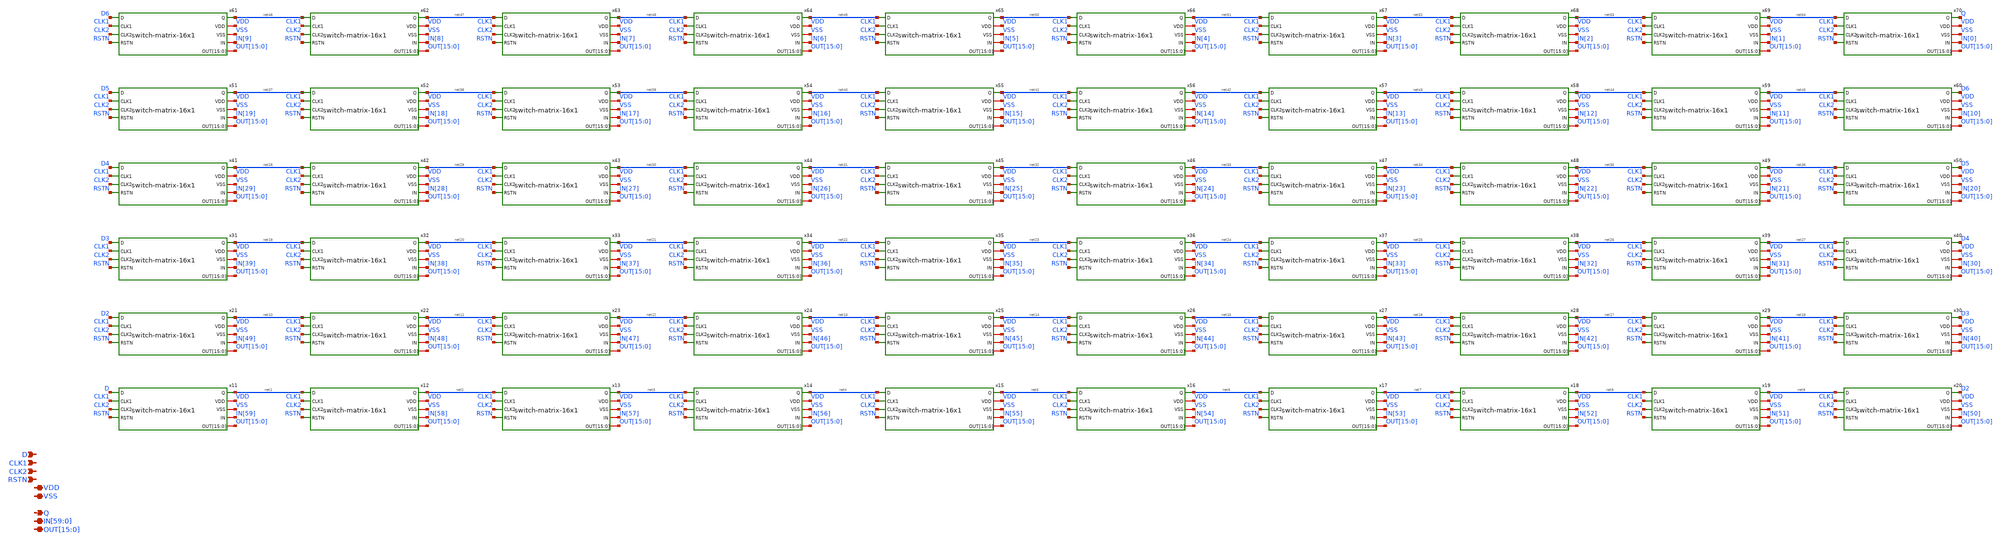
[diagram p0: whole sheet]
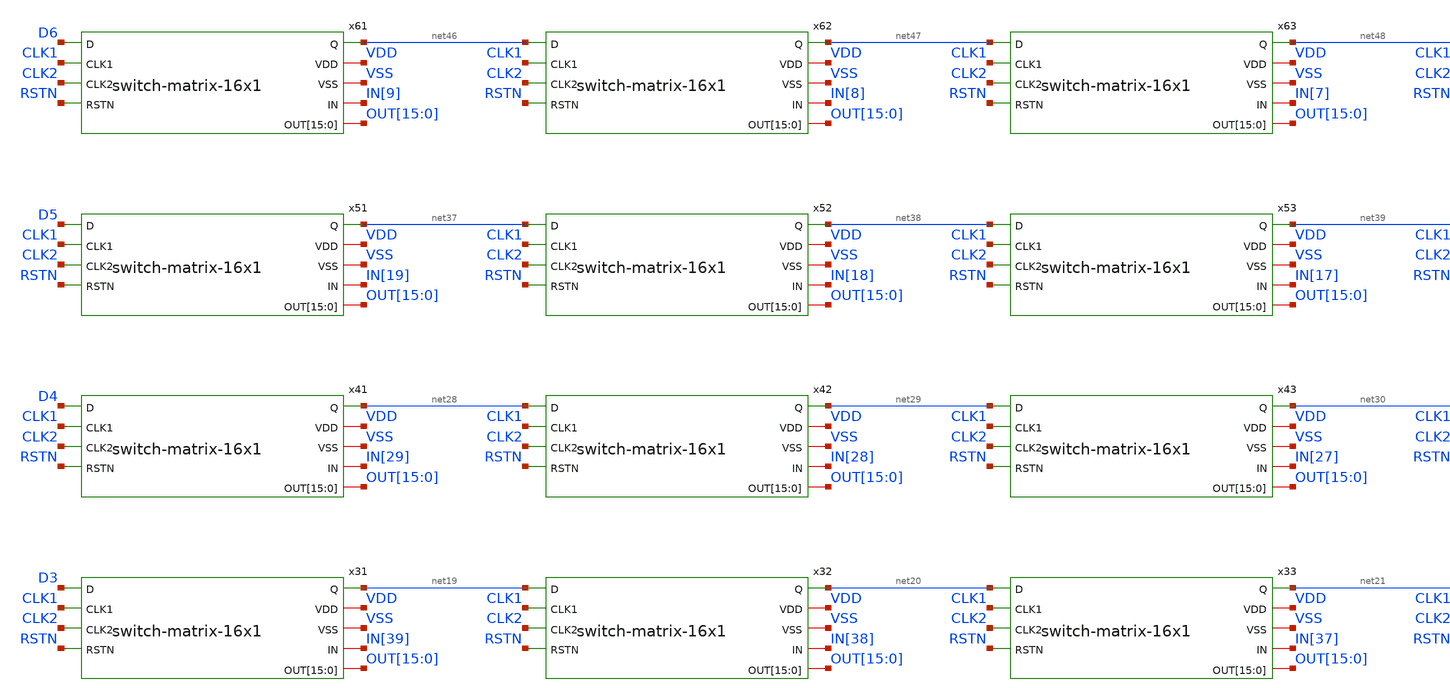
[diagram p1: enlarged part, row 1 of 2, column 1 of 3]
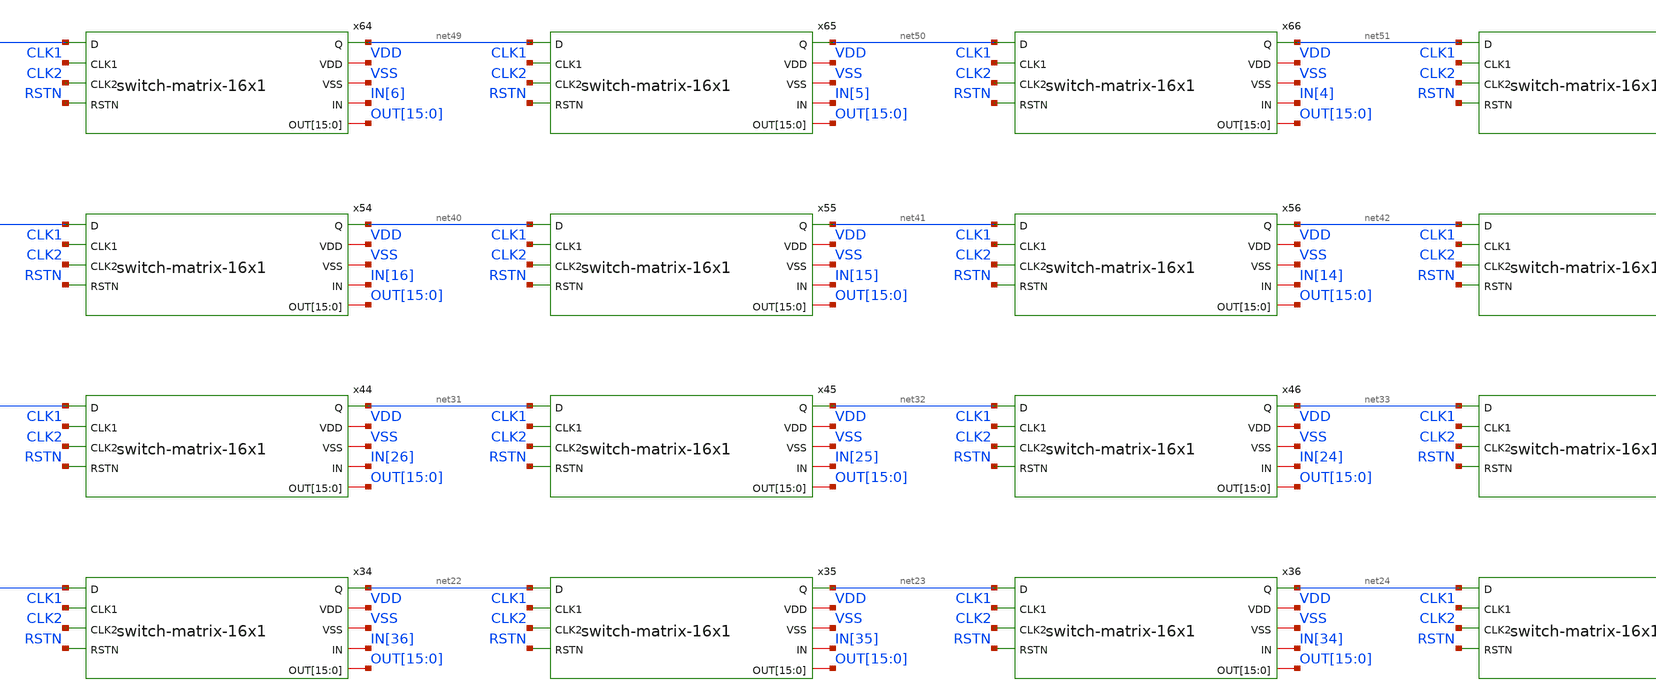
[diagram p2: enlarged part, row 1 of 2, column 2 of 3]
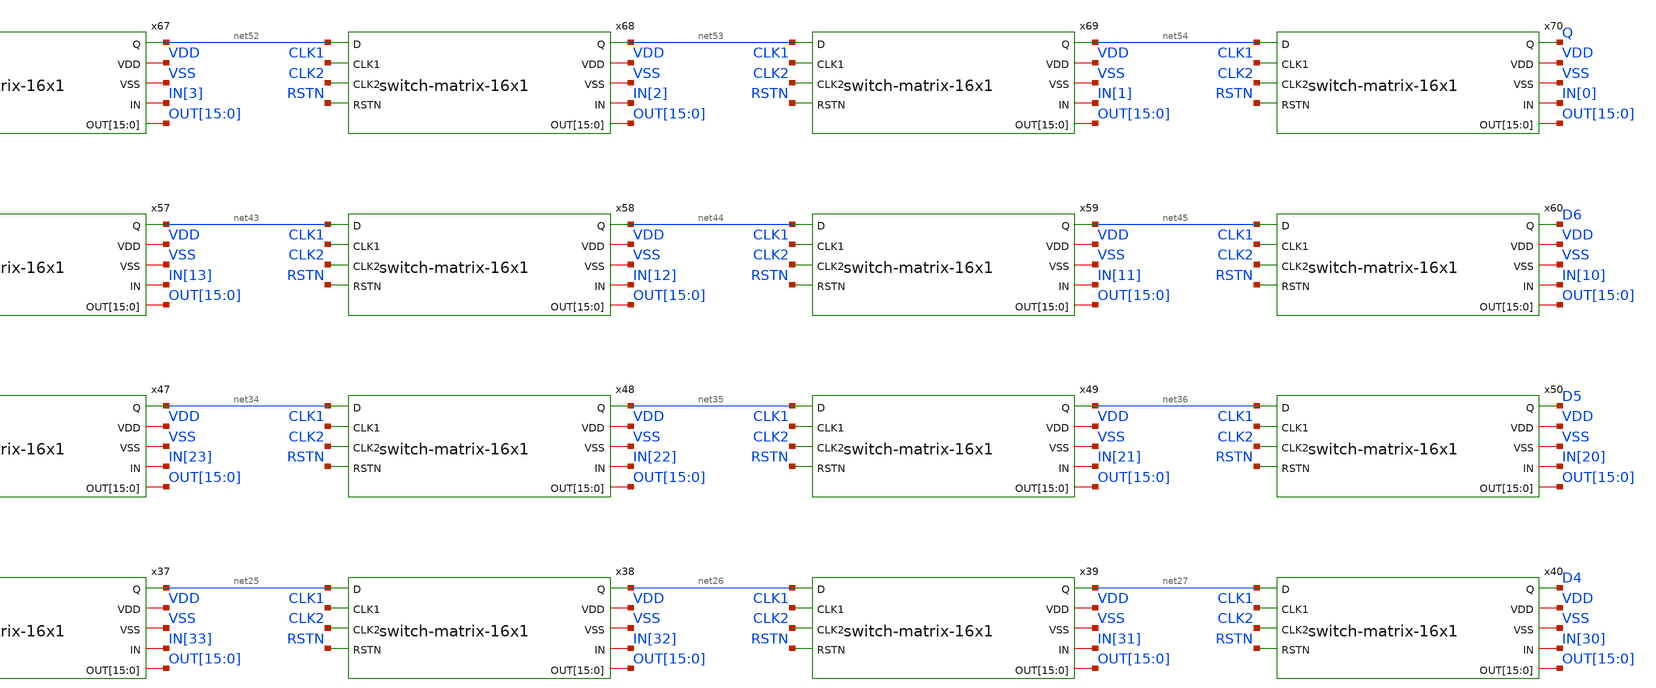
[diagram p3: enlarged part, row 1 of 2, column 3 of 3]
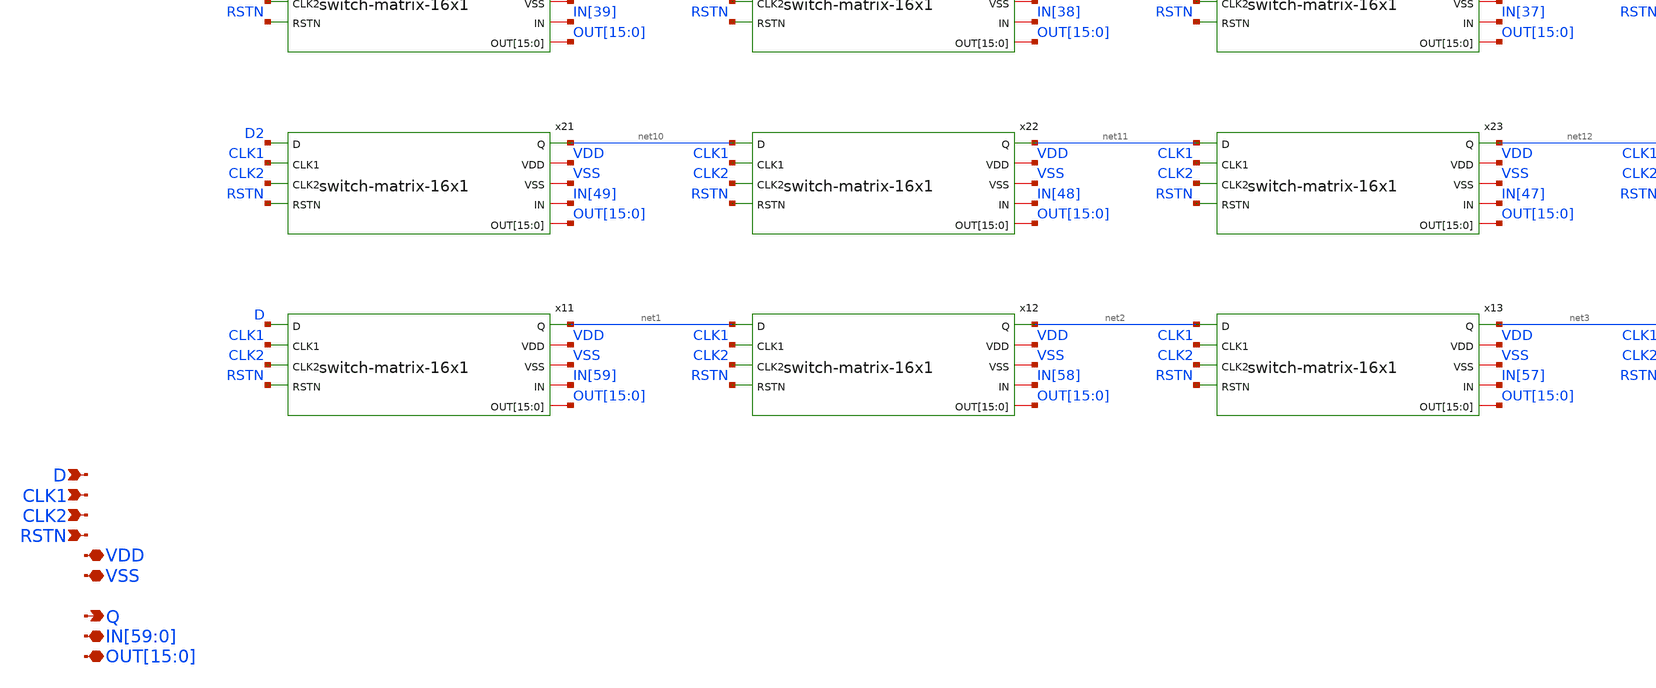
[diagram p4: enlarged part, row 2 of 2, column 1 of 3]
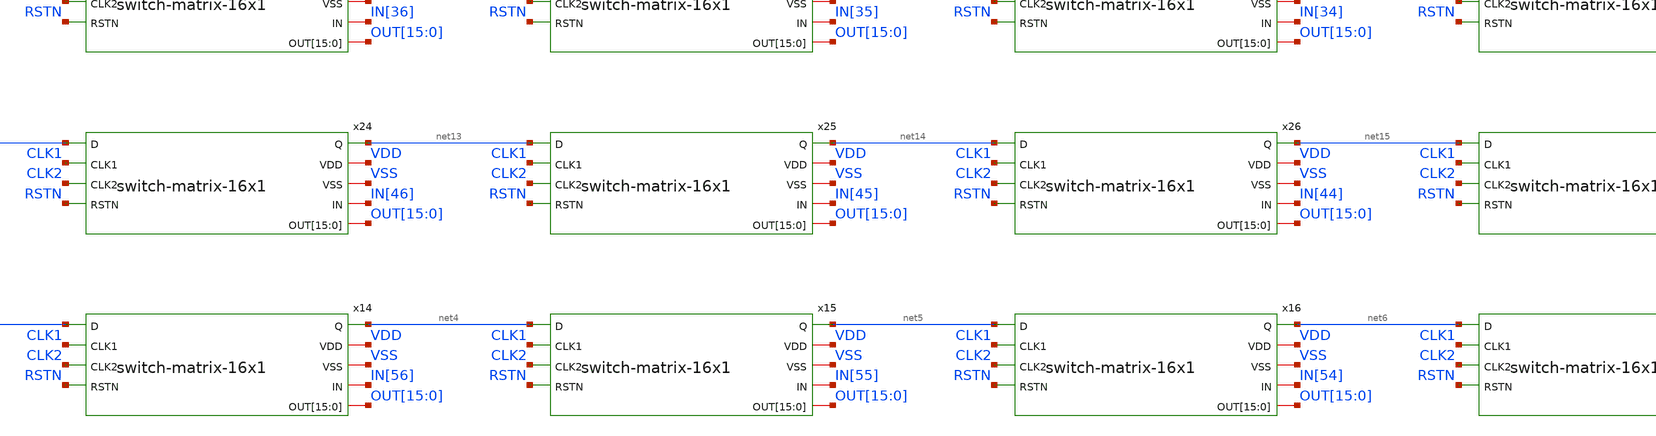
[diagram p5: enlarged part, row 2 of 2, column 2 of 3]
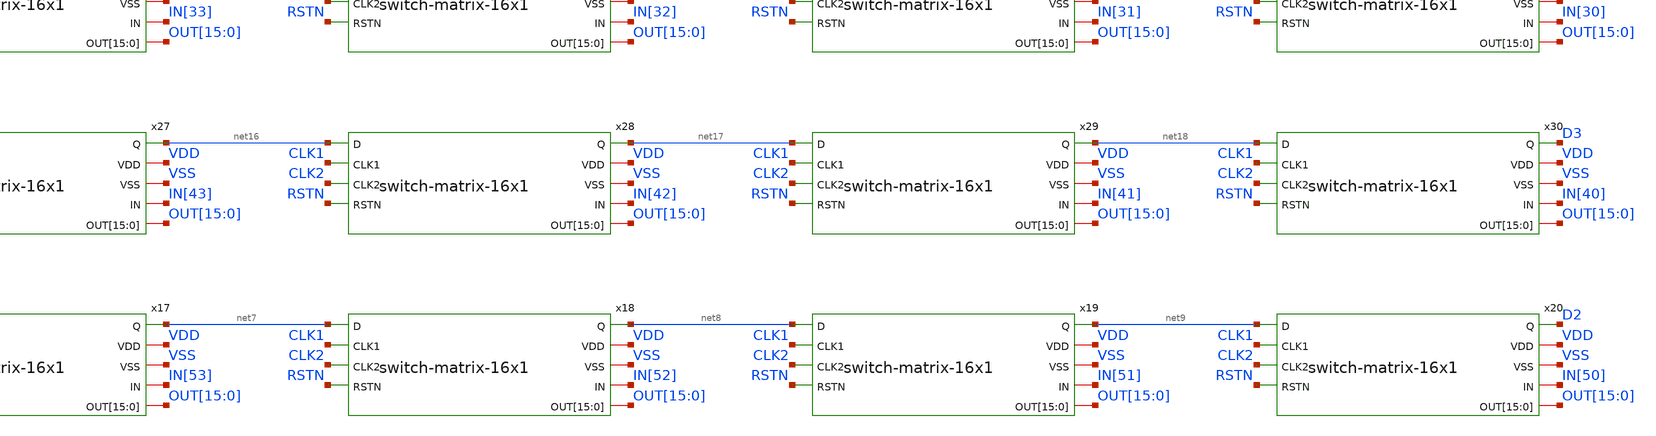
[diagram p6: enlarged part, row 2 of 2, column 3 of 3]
** sch_path: designs/libs/core_switch-matrix/switch-matrix-16x70/switch-matrix-16x70.sch
**.subckt switch-matrix-16x70 VDD VSS RSTN CLK1 CLK2 D
*+ IN[59],IN[58],IN[57],IN[56],IN[55],IN[54],IN[53],IN[52],IN[51],IN[50],IN[49],IN[48],IN[47],IN[46],IN[45],IN[44],IN[43],IN[42],IN[41],IN[40],IN[39],IN[38],IN[37],IN[36],IN[35],IN[34],IN[33],IN[32],IN[31],IN[30],IN[29],IN[28],IN[27],IN[26],IN[25],IN[24],IN[23],IN[22],IN[21],IN[20],IN[19],IN[18],IN[17],IN[16],IN[15],IN[14],IN[13],IN[12],IN[11],IN[10],IN[9],IN[8],IN[7],IN[6],IN[5],IN[4],IN[3],IN[2],IN[1],IN[0]
*+ OUT[15],OUT[14],OUT[13],OUT[12],OUT[11],OUT[10],OUT[9],OUT[8],OUT[7],OUT[6],OUT[5],OUT[4],OUT[3],OUT[2],OUT[1],OUT[0] Q
*.iopin VDD
*.iopin VSS
*.ipin RSTN
*.ipin CLK1
*.ipin CLK2
*.ipin D
*.iopin
*+ IN[59],IN[58],IN[57],IN[56],IN[55],IN[54],IN[53],IN[52],IN[51],IN[50],IN[49],IN[48],IN[47],IN[46],IN[45],IN[44],IN[43],IN[42],IN[41],IN[40],IN[39],IN[38],IN[37],IN[36],IN[35],IN[34],IN[33],IN[32],IN[31],IN[30],IN[29],IN[28],IN[27],IN[26],IN[25],IN[24],IN[23],IN[22],IN[21],IN[20],IN[19],IN[18],IN[17],IN[16],IN[15],IN[14],IN[13],IN[12],IN[11],IN[10],IN[9],IN[8],IN[7],IN[6],IN[5],IN[4],IN[3],IN[2],IN[1],IN[0]
*.iopin
*+ OUT[15],OUT[14],OUT[13],OUT[12],OUT[11],OUT[10],OUT[9],OUT[8],OUT[7],OUT[6],OUT[5],OUT[4],OUT[3],OUT[2],OUT[1],OUT[0]
*.opin Q
x11 net1 VDD VSS IN[59] OUT[15] OUT[14] OUT[13] OUT[12] OUT[11] OUT[10] OUT[9] OUT[8] OUT[7] OUT[6]
+ OUT[5] OUT[4] OUT[3] OUT[2] OUT[1] OUT[0] D CLK1 CLK2 RSTN switch-matrix-16x1
x12 net2 VDD VSS IN[58] OUT[15] OUT[14] OUT[13] OUT[12] OUT[11] OUT[10] OUT[9] OUT[8] OUT[7] OUT[6]
+ OUT[5] OUT[4] OUT[3] OUT[2] OUT[1] OUT[0] net1 CLK1 CLK2 RSTN switch-matrix-16x1
x13 net3 VDD VSS IN[57] OUT[15] OUT[14] OUT[13] OUT[12] OUT[11] OUT[10] OUT[9] OUT[8] OUT[7] OUT[6]
+ OUT[5] OUT[4] OUT[3] OUT[2] OUT[1] OUT[0] net2 CLK1 CLK2 RSTN switch-matrix-16x1
x14 net4 VDD VSS IN[56] OUT[15] OUT[14] OUT[13] OUT[12] OUT[11] OUT[10] OUT[9] OUT[8] OUT[7] OUT[6]
+ OUT[5] OUT[4] OUT[3] OUT[2] OUT[1] OUT[0] net3 CLK1 CLK2 RSTN switch-matrix-16x1
x15 net5 VDD VSS IN[55] OUT[15] OUT[14] OUT[13] OUT[12] OUT[11] OUT[10] OUT[9] OUT[8] OUT[7] OUT[6]
+ OUT[5] OUT[4] OUT[3] OUT[2] OUT[1] OUT[0] net4 CLK1 CLK2 RSTN switch-matrix-16x1
x16 net6 VDD VSS IN[54] OUT[15] OUT[14] OUT[13] OUT[12] OUT[11] OUT[10] OUT[9] OUT[8] OUT[7] OUT[6]
+ OUT[5] OUT[4] OUT[3] OUT[2] OUT[1] OUT[0] net5 CLK1 CLK2 RSTN switch-matrix-16x1
x17 net7 VDD VSS IN[53] OUT[15] OUT[14] OUT[13] OUT[12] OUT[11] OUT[10] OUT[9] OUT[8] OUT[7] OUT[6]
+ OUT[5] OUT[4] OUT[3] OUT[2] OUT[1] OUT[0] net6 CLK1 CLK2 RSTN switch-matrix-16x1
x18 net8 VDD VSS IN[52] OUT[15] OUT[14] OUT[13] OUT[12] OUT[11] OUT[10] OUT[9] OUT[8] OUT[7] OUT[6]
+ OUT[5] OUT[4] OUT[3] OUT[2] OUT[1] OUT[0] net7 CLK1 CLK2 RSTN switch-matrix-16x1
x19 net9 VDD VSS IN[51] OUT[15] OUT[14] OUT[13] OUT[12] OUT[11] OUT[10] OUT[9] OUT[8] OUT[7] OUT[6]
+ OUT[5] OUT[4] OUT[3] OUT[2] OUT[1] OUT[0] net8 CLK1 CLK2 RSTN switch-matrix-16x1
x20 D2 VDD VSS IN[50] OUT[15] OUT[14] OUT[13] OUT[12] OUT[11] OUT[10] OUT[9] OUT[8] OUT[7] OUT[6]
+ OUT[5] OUT[4] OUT[3] OUT[2] OUT[1] OUT[0] net9 CLK1 CLK2 RSTN switch-matrix-16x1
x21 net10 VDD VSS IN[49] OUT[15] OUT[14] OUT[13] OUT[12] OUT[11] OUT[10] OUT[9] OUT[8] OUT[7] OUT[6]
+ OUT[5] OUT[4] OUT[3] OUT[2] OUT[1] OUT[0] D2 CLK1 CLK2 RSTN switch-matrix-16x1
x22 net11 VDD VSS IN[48] OUT[15] OUT[14] OUT[13] OUT[12] OUT[11] OUT[10] OUT[9] OUT[8] OUT[7] OUT[6]
+ OUT[5] OUT[4] OUT[3] OUT[2] OUT[1] OUT[0] net10 CLK1 CLK2 RSTN switch-matrix-16x1
x23 net12 VDD VSS IN[47] OUT[15] OUT[14] OUT[13] OUT[12] OUT[11] OUT[10] OUT[9] OUT[8] OUT[7] OUT[6]
+ OUT[5] OUT[4] OUT[3] OUT[2] OUT[1] OUT[0] net11 CLK1 CLK2 RSTN switch-matrix-16x1
x24 net13 VDD VSS IN[46] OUT[15] OUT[14] OUT[13] OUT[12] OUT[11] OUT[10] OUT[9] OUT[8] OUT[7] OUT[6]
+ OUT[5] OUT[4] OUT[3] OUT[2] OUT[1] OUT[0] net12 CLK1 CLK2 RSTN switch-matrix-16x1
x25 net14 VDD VSS IN[45] OUT[15] OUT[14] OUT[13] OUT[12] OUT[11] OUT[10] OUT[9] OUT[8] OUT[7] OUT[6]
+ OUT[5] OUT[4] OUT[3] OUT[2] OUT[1] OUT[0] net13 CLK1 CLK2 RSTN switch-matrix-16x1
x26 net15 VDD VSS IN[44] OUT[15] OUT[14] OUT[13] OUT[12] OUT[11] OUT[10] OUT[9] OUT[8] OUT[7] OUT[6]
+ OUT[5] OUT[4] OUT[3] OUT[2] OUT[1] OUT[0] net14 CLK1 CLK2 RSTN switch-matrix-16x1
x27 net16 VDD VSS IN[43] OUT[15] OUT[14] OUT[13] OUT[12] OUT[11] OUT[10] OUT[9] OUT[8] OUT[7] OUT[6]
+ OUT[5] OUT[4] OUT[3] OUT[2] OUT[1] OUT[0] net15 CLK1 CLK2 RSTN switch-matrix-16x1
x28 net17 VDD VSS IN[42] OUT[15] OUT[14] OUT[13] OUT[12] OUT[11] OUT[10] OUT[9] OUT[8] OUT[7] OUT[6]
+ OUT[5] OUT[4] OUT[3] OUT[2] OUT[1] OUT[0] net16 CLK1 CLK2 RSTN switch-matrix-16x1
x29 net18 VDD VSS IN[41] OUT[15] OUT[14] OUT[13] OUT[12] OUT[11] OUT[10] OUT[9] OUT[8] OUT[7] OUT[6]
+ OUT[5] OUT[4] OUT[3] OUT[2] OUT[1] OUT[0] net17 CLK1 CLK2 RSTN switch-matrix-16x1
x30 D3 VDD VSS IN[40] OUT[15] OUT[14] OUT[13] OUT[12] OUT[11] OUT[10] OUT[9] OUT[8] OUT[7] OUT[6]
+ OUT[5] OUT[4] OUT[3] OUT[2] OUT[1] OUT[0] net18 CLK1 CLK2 RSTN switch-matrix-16x1
x31 net19 VDD VSS IN[39] OUT[15] OUT[14] OUT[13] OUT[12] OUT[11] OUT[10] OUT[9] OUT[8] OUT[7] OUT[6]
+ OUT[5] OUT[4] OUT[3] OUT[2] OUT[1] OUT[0] D3 CLK1 CLK2 RSTN switch-matrix-16x1
x32 net20 VDD VSS IN[38] OUT[15] OUT[14] OUT[13] OUT[12] OUT[11] OUT[10] OUT[9] OUT[8] OUT[7] OUT[6]
+ OUT[5] OUT[4] OUT[3] OUT[2] OUT[1] OUT[0] net19 CLK1 CLK2 RSTN switch-matrix-16x1
x33 net21 VDD VSS IN[37] OUT[15] OUT[14] OUT[13] OUT[12] OUT[11] OUT[10] OUT[9] OUT[8] OUT[7] OUT[6]
+ OUT[5] OUT[4] OUT[3] OUT[2] OUT[1] OUT[0] net20 CLK1 CLK2 RSTN switch-matrix-16x1
x34 net22 VDD VSS IN[36] OUT[15] OUT[14] OUT[13] OUT[12] OUT[11] OUT[10] OUT[9] OUT[8] OUT[7] OUT[6]
+ OUT[5] OUT[4] OUT[3] OUT[2] OUT[1] OUT[0] net21 CLK1 CLK2 RSTN switch-matrix-16x1
x35 net23 VDD VSS IN[35] OUT[15] OUT[14] OUT[13] OUT[12] OUT[11] OUT[10] OUT[9] OUT[8] OUT[7] OUT[6]
+ OUT[5] OUT[4] OUT[3] OUT[2] OUT[1] OUT[0] net22 CLK1 CLK2 RSTN switch-matrix-16x1
x36 net24 VDD VSS IN[34] OUT[15] OUT[14] OUT[13] OUT[12] OUT[11] OUT[10] OUT[9] OUT[8] OUT[7] OUT[6]
+ OUT[5] OUT[4] OUT[3] OUT[2] OUT[1] OUT[0] net23 CLK1 CLK2 RSTN switch-matrix-16x1
x37 net25 VDD VSS IN[33] OUT[15] OUT[14] OUT[13] OUT[12] OUT[11] OUT[10] OUT[9] OUT[8] OUT[7] OUT[6]
+ OUT[5] OUT[4] OUT[3] OUT[2] OUT[1] OUT[0] net24 CLK1 CLK2 RSTN switch-matrix-16x1
x38 net26 VDD VSS IN[32] OUT[15] OUT[14] OUT[13] OUT[12] OUT[11] OUT[10] OUT[9] OUT[8] OUT[7] OUT[6]
+ OUT[5] OUT[4] OUT[3] OUT[2] OUT[1] OUT[0] net25 CLK1 CLK2 RSTN switch-matrix-16x1
x39 net27 VDD VSS IN[31] OUT[15] OUT[14] OUT[13] OUT[12] OUT[11] OUT[10] OUT[9] OUT[8] OUT[7] OUT[6]
+ OUT[5] OUT[4] OUT[3] OUT[2] OUT[1] OUT[0] net26 CLK1 CLK2 RSTN switch-matrix-16x1
x40 D4 VDD VSS IN[30] OUT[15] OUT[14] OUT[13] OUT[12] OUT[11] OUT[10] OUT[9] OUT[8] OUT[7] OUT[6]
+ OUT[5] OUT[4] OUT[3] OUT[2] OUT[1] OUT[0] net27 CLK1 CLK2 RSTN switch-matrix-16x1
x41 net28 VDD VSS IN[29] OUT[15] OUT[14] OUT[13] OUT[12] OUT[11] OUT[10] OUT[9] OUT[8] OUT[7] OUT[6]
+ OUT[5] OUT[4] OUT[3] OUT[2] OUT[1] OUT[0] D4 CLK1 CLK2 RSTN switch-matrix-16x1
x42 net29 VDD VSS IN[28] OUT[15] OUT[14] OUT[13] OUT[12] OUT[11] OUT[10] OUT[9] OUT[8] OUT[7] OUT[6]
+ OUT[5] OUT[4] OUT[3] OUT[2] OUT[1] OUT[0] net28 CLK1 CLK2 RSTN switch-matrix-16x1
x43 net30 VDD VSS IN[27] OUT[15] OUT[14] OUT[13] OUT[12] OUT[11] OUT[10] OUT[9] OUT[8] OUT[7] OUT[6]
+ OUT[5] OUT[4] OUT[3] OUT[2] OUT[1] OUT[0] net29 CLK1 CLK2 RSTN switch-matrix-16x1
x44 net31 VDD VSS IN[26] OUT[15] OUT[14] OUT[13] OUT[12] OUT[11] OUT[10] OUT[9] OUT[8] OUT[7] OUT[6]
+ OUT[5] OUT[4] OUT[3] OUT[2] OUT[1] OUT[0] net30 CLK1 CLK2 RSTN switch-matrix-16x1
x45 net32 VDD VSS IN[25] OUT[15] OUT[14] OUT[13] OUT[12] OUT[11] OUT[10] OUT[9] OUT[8] OUT[7] OUT[6]
+ OUT[5] OUT[4] OUT[3] OUT[2] OUT[1] OUT[0] net31 CLK1 CLK2 RSTN switch-matrix-16x1
x46 net33 VDD VSS IN[24] OUT[15] OUT[14] OUT[13] OUT[12] OUT[11] OUT[10] OUT[9] OUT[8] OUT[7] OUT[6]
+ OUT[5] OUT[4] OUT[3] OUT[2] OUT[1] OUT[0] net32 CLK1 CLK2 RSTN switch-matrix-16x1
x47 net34 VDD VSS IN[23] OUT[15] OUT[14] OUT[13] OUT[12] OUT[11] OUT[10] OUT[9] OUT[8] OUT[7] OUT[6]
+ OUT[5] OUT[4] OUT[3] OUT[2] OUT[1] OUT[0] net33 CLK1 CLK2 RSTN switch-matrix-16x1
x48 net35 VDD VSS IN[22] OUT[15] OUT[14] OUT[13] OUT[12] OUT[11] OUT[10] OUT[9] OUT[8] OUT[7] OUT[6]
+ OUT[5] OUT[4] OUT[3] OUT[2] OUT[1] OUT[0] net34 CLK1 CLK2 RSTN switch-matrix-16x1
x49 net36 VDD VSS IN[21] OUT[15] OUT[14] OUT[13] OUT[12] OUT[11] OUT[10] OUT[9] OUT[8] OUT[7] OUT[6]
+ OUT[5] OUT[4] OUT[3] OUT[2] OUT[1] OUT[0] net35 CLK1 CLK2 RSTN switch-matrix-16x1
x50 D5 VDD VSS IN[20] OUT[15] OUT[14] OUT[13] OUT[12] OUT[11] OUT[10] OUT[9] OUT[8] OUT[7] OUT[6]
+ OUT[5] OUT[4] OUT[3] OUT[2] OUT[1] OUT[0] net36 CLK1 CLK2 RSTN switch-matrix-16x1
x51 net37 VDD VSS IN[19] OUT[15] OUT[14] OUT[13] OUT[12] OUT[11] OUT[10] OUT[9] OUT[8] OUT[7] OUT[6]
+ OUT[5] OUT[4] OUT[3] OUT[2] OUT[1] OUT[0] D5 CLK1 CLK2 RSTN switch-matrix-16x1
x52 net38 VDD VSS IN[18] OUT[15] OUT[14] OUT[13] OUT[12] OUT[11] OUT[10] OUT[9] OUT[8] OUT[7] OUT[6]
+ OUT[5] OUT[4] OUT[3] OUT[2] OUT[1] OUT[0] net37 CLK1 CLK2 RSTN switch-matrix-16x1
x53 net39 VDD VSS IN[17] OUT[15] OUT[14] OUT[13] OUT[12] OUT[11] OUT[10] OUT[9] OUT[8] OUT[7] OUT[6]
+ OUT[5] OUT[4] OUT[3] OUT[2] OUT[1] OUT[0] net38 CLK1 CLK2 RSTN switch-matrix-16x1
x54 net40 VDD VSS IN[16] OUT[15] OUT[14] OUT[13] OUT[12] OUT[11] OUT[10] OUT[9] OUT[8] OUT[7] OUT[6]
+ OUT[5] OUT[4] OUT[3] OUT[2] OUT[1] OUT[0] net39 CLK1 CLK2 RSTN switch-matrix-16x1
x55 net41 VDD VSS IN[15] OUT[15] OUT[14] OUT[13] OUT[12] OUT[11] OUT[10] OUT[9] OUT[8] OUT[7] OUT[6]
+ OUT[5] OUT[4] OUT[3] OUT[2] OUT[1] OUT[0] net40 CLK1 CLK2 RSTN switch-matrix-16x1
x56 net42 VDD VSS IN[14] OUT[15] OUT[14] OUT[13] OUT[12] OUT[11] OUT[10] OUT[9] OUT[8] OUT[7] OUT[6]
+ OUT[5] OUT[4] OUT[3] OUT[2] OUT[1] OUT[0] net41 CLK1 CLK2 RSTN switch-matrix-16x1
x57 net43 VDD VSS IN[13] OUT[15] OUT[14] OUT[13] OUT[12] OUT[11] OUT[10] OUT[9] OUT[8] OUT[7] OUT[6]
+ OUT[5] OUT[4] OUT[3] OUT[2] OUT[1] OUT[0] net42 CLK1 CLK2 RSTN switch-matrix-16x1
x58 net44 VDD VSS IN[12] OUT[15] OUT[14] OUT[13] OUT[12] OUT[11] OUT[10] OUT[9] OUT[8] OUT[7] OUT[6]
+ OUT[5] OUT[4] OUT[3] OUT[2] OUT[1] OUT[0] net43 CLK1 CLK2 RSTN switch-matrix-16x1
x59 net45 VDD VSS IN[11] OUT[15] OUT[14] OUT[13] OUT[12] OUT[11] OUT[10] OUT[9] OUT[8] OUT[7] OUT[6]
+ OUT[5] OUT[4] OUT[3] OUT[2] OUT[1] OUT[0] net44 CLK1 CLK2 RSTN switch-matrix-16x1
x60 D6 VDD VSS IN[10] OUT[15] OUT[14] OUT[13] OUT[12] OUT[11] OUT[10] OUT[9] OUT[8] OUT[7] OUT[6]
+ OUT[5] OUT[4] OUT[3] OUT[2] OUT[1] OUT[0] net45 CLK1 CLK2 RSTN switch-matrix-16x1
x61 net46 VDD VSS IN[9] OUT[15] OUT[14] OUT[13] OUT[12] OUT[11] OUT[10] OUT[9] OUT[8] OUT[7] OUT[6]
+ OUT[5] OUT[4] OUT[3] OUT[2] OUT[1] OUT[0] D6 CLK1 CLK2 RSTN switch-matrix-16x1
x62 net47 VDD VSS IN[8] OUT[15] OUT[14] OUT[13] OUT[12] OUT[11] OUT[10] OUT[9] OUT[8] OUT[7] OUT[6]
+ OUT[5] OUT[4] OUT[3] OUT[2] OUT[1] OUT[0] net46 CLK1 CLK2 RSTN switch-matrix-16x1
x63 net48 VDD VSS IN[7] OUT[15] OUT[14] OUT[13] OUT[12] OUT[11] OUT[10] OUT[9] OUT[8] OUT[7] OUT[6]
+ OUT[5] OUT[4] OUT[3] OUT[2] OUT[1] OUT[0] net47 CLK1 CLK2 RSTN switch-matrix-16x1
x64 net49 VDD VSS IN[6] OUT[15] OUT[14] OUT[13] OUT[12] OUT[11] OUT[10] OUT[9] OUT[8] OUT[7] OUT[6]
+ OUT[5] OUT[4] OUT[3] OUT[2] OUT[1] OUT[0] net48 CLK1 CLK2 RSTN switch-matrix-16x1
x65 net50 VDD VSS IN[5] OUT[15] OUT[14] OUT[13] OUT[12] OUT[11] OUT[10] OUT[9] OUT[8] OUT[7] OUT[6]
+ OUT[5] OUT[4] OUT[3] OUT[2] OUT[1] OUT[0] net49 CLK1 CLK2 RSTN switch-matrix-16x1
x66 net51 VDD VSS IN[4] OUT[15] OUT[14] OUT[13] OUT[12] OUT[11] OUT[10] OUT[9] OUT[8] OUT[7] OUT[6]
+ OUT[5] OUT[4] OUT[3] OUT[2] OUT[1] OUT[0] net50 CLK1 CLK2 RSTN switch-matrix-16x1
x67 net52 VDD VSS IN[3] OUT[15] OUT[14] OUT[13] OUT[12] OUT[11] OUT[10] OUT[9] OUT[8] OUT[7] OUT[6]
+ OUT[5] OUT[4] OUT[3] OUT[2] OUT[1] OUT[0] net51 CLK1 CLK2 RSTN switch-matrix-16x1
x68 net53 VDD VSS IN[2] OUT[15] OUT[14] OUT[13] OUT[12] OUT[11] OUT[10] OUT[9] OUT[8] OUT[7] OUT[6]
+ OUT[5] OUT[4] OUT[3] OUT[2] OUT[1] OUT[0] net52 CLK1 CLK2 RSTN switch-matrix-16x1
x69 net54 VDD VSS IN[1] OUT[15] OUT[14] OUT[13] OUT[12] OUT[11] OUT[10] OUT[9] OUT[8] OUT[7] OUT[6]
+ OUT[5] OUT[4] OUT[3] OUT[2] OUT[1] OUT[0] net53 CLK1 CLK2 RSTN switch-matrix-16x1
x70 Q VDD VSS IN[0] OUT[15] OUT[14] OUT[13] OUT[12] OUT[11] OUT[10] OUT[9] OUT[8] OUT[7] OUT[6]
+ OUT[5] OUT[4] OUT[3] OUT[2] OUT[1] OUT[0] net54 CLK1 CLK2 RSTN switch-matrix-16x1
**.ends
.end
